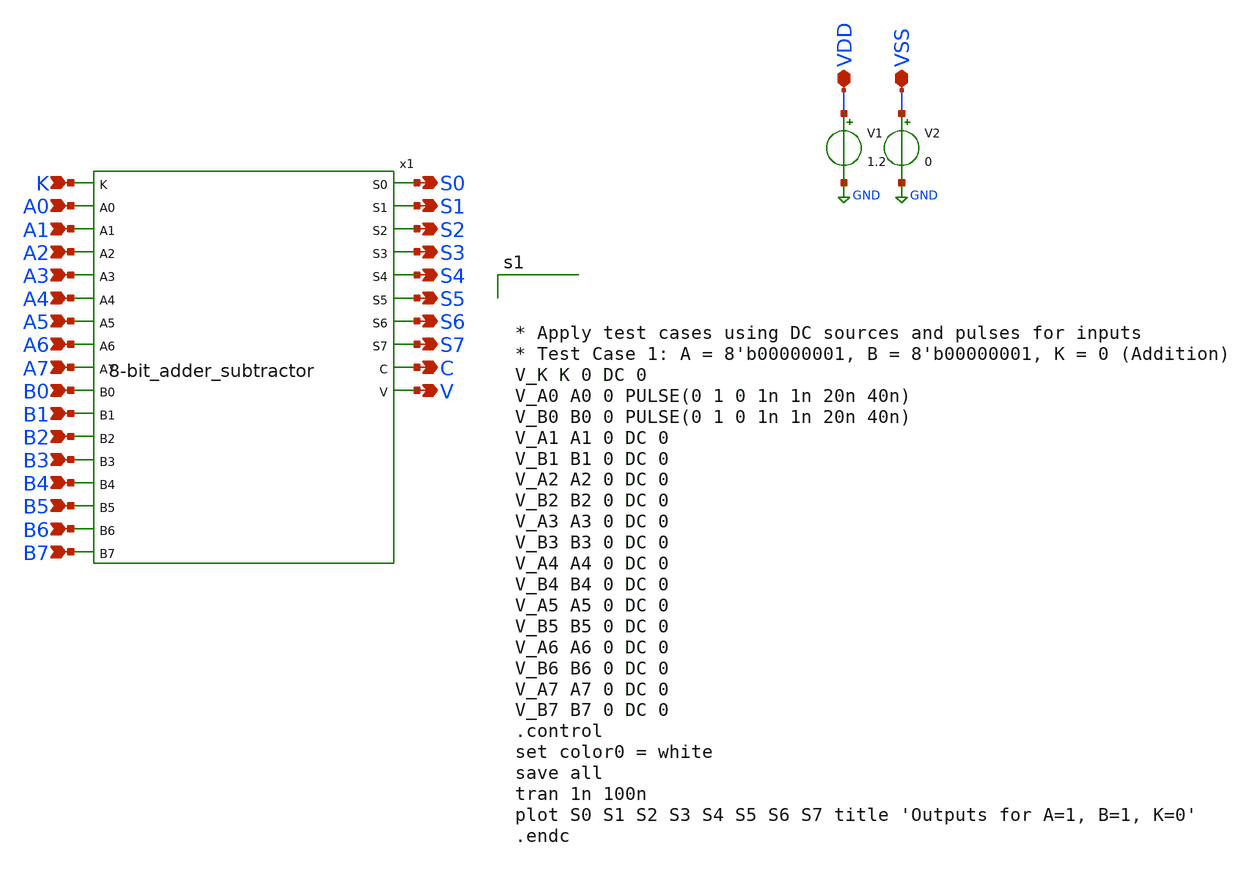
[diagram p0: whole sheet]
** sch_path: design/xschem/tb_adder_substractor.sch
**.subckt tb_adder_substractor K A0 A1 B1 A2 B2 A3 B3 A4 B4 A5 B5 A6 B6 A7 B7 B0 S6 S7 S3 S4 S5 S0
*+ S1 S2 C V VDD VSS
*.ipin K
*.ipin A0
*.ipin A1
*.ipin B1
*.ipin A2
*.ipin B2
*.ipin A3
*.ipin B3
*.ipin A4
*.ipin B4
*.ipin A5
*.ipin B5
*.ipin A6
*.ipin B6
*.ipin A7
*.ipin B7
*.ipin B0
*.opin S6
*.opin S7
*.opin S3
*.opin S4
*.opin S5
*.opin S0
*.opin S1
*.opin S2
*.opin C
*.opin V
*.iopin VDD
*.iopin VSS
x1 K A0 S0 B0 A1 S1 B1 A2 S2 B2 A3 S3 B3 A4 S4 B4 A5 S5 B5 A6 S6 B6 A7 S7 B7 C V
+ 8-bit_adder_subtractor
V1 VDD GND 1.2
V2 VSS GND 0
**** begin user architecture code

** opencircuitdesign pdks install
.lib $::SKYWATER_MODELS/sky130.lib.spice tt_mm





* Apply test cases using DC sources and pulses for inputs
* Test Case 1: A = 8'b00000001, B = 8'b00000001, K = 0 (Addition)
V_K K 0 DC 0
V_A0 A0 0 PULSE(0 1 0 1n 1n 20n 40n)
V_B0 B0 0 PULSE(0 1 0 1n 1n 20n 40n)
V_A1 A1 0 DC 0
V_B1 B1 0 DC 0
V_A2 A2 0 DC 0
V_B2 B2 0 DC 0
V_A3 A3 0 DC 0
V_B3 B3 0 DC 0
V_A4 A4 0 DC 0
V_B4 B4 0 DC 0
V_A5 A5 0 DC 0
V_B5 B5 0 DC 0
V_A6 A6 0 DC 0
V_B6 B6 0 DC 0
V_A7 A7 0 DC 0
V_B7 B7 0 DC 0
.control
set color0 = white
save all
tran 1n 100n
plot S0 S1 S2 S3 S4 S5 S6 S7 title 'Outputs for A=1, B=1, K=0'
.endc


**** end user architecture code
**.ends
.GLOBAL GND
.end
